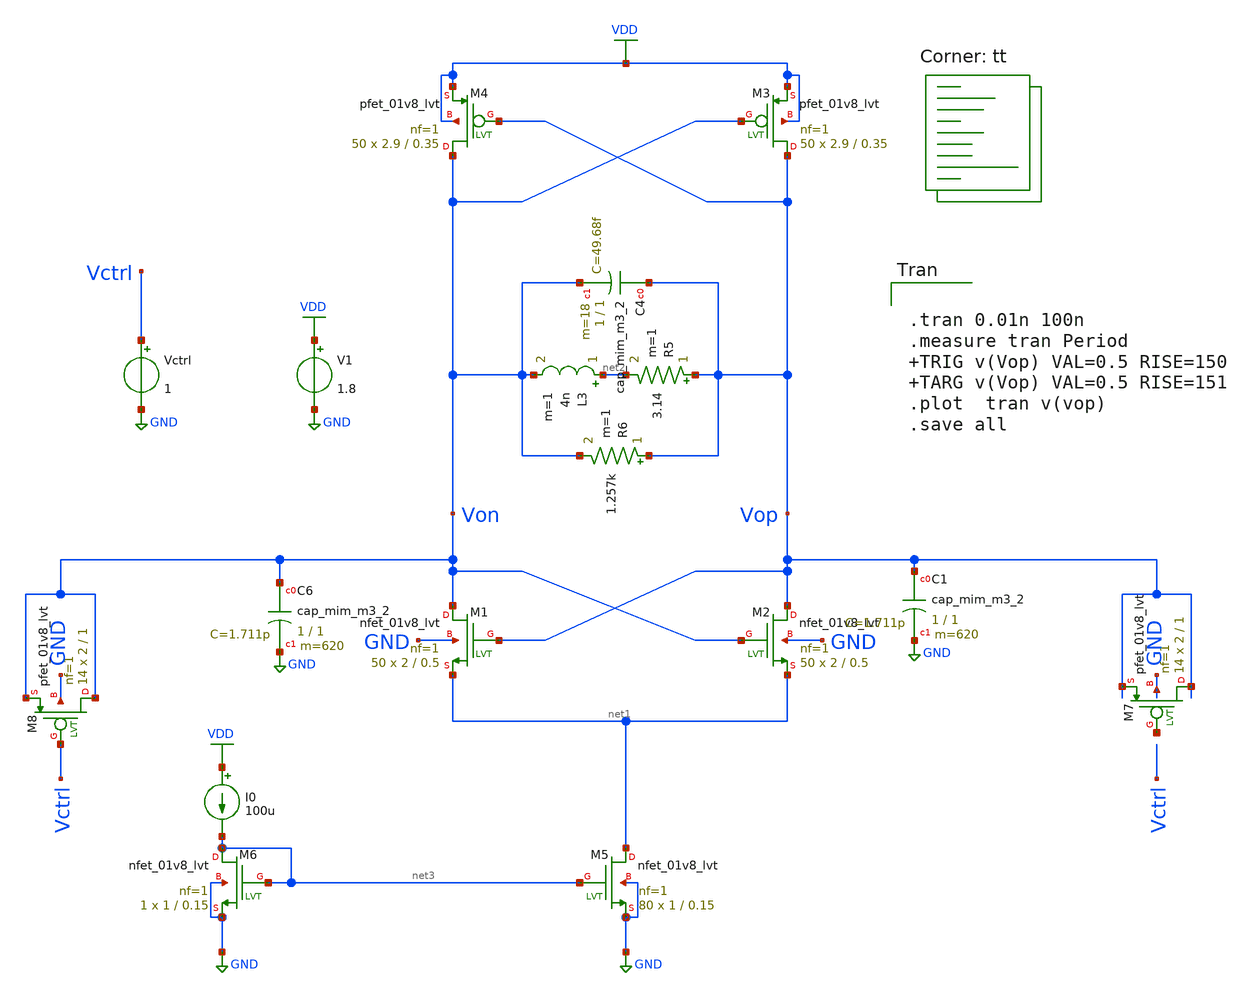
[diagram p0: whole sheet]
** sch_path: pll/lc_vco_lib/5_lc_vco_Hossam_Tarek/xschem/lc_osc_complementary.sch
**.subckt lc_osc_complementary
XM1 Von Vop net1 GND sky130_fd_pr__nfet_01v8_lvt L=0.5 W=2 nf=1 ad='int((nf+1)/2) * W/nf * 0.29' as='int((nf+2)/2) * W/nf * 0.29'
+ pd='2*int((nf+1)/2) * (W/nf + 0.29)' ps='2*int((nf+2)/2) * (W/nf + 0.29)' nrd='0.29 / W' nrs='0.29 / W'
+ sa=0 sb=0 sd=0 mult=50 m=50
XM2 Vop Von net1 GND sky130_fd_pr__nfet_01v8_lvt L=0.5 W=2 nf=1 ad='int((nf+1)/2) * W/nf * 0.29' as='int((nf+2)/2) * W/nf * 0.29'
+ pd='2*int((nf+1)/2) * (W/nf + 0.29)' ps='2*int((nf+2)/2) * (W/nf + 0.29)' nrd='0.29 / W' nrs='0.29 / W'
+ sa=0 sb=0 sd=0 mult=50 m=50
V1 VDD GND 1.8
XC6 Von GND sky130_fd_pr__cap_mim_m3_2 W=1 L=1 MF=620 m=620
XC1 Vop GND sky130_fd_pr__cap_mim_m3_2 W=1 L=1 MF=620 m=620
L3 net2 Von 4n m=1
R5 Vop net2 3.14 m=1
R6 Vop Von 1.257k m=1
XC4 Vop Von sky130_fd_pr__cap_mim_m3_2 W=1 L=1 MF=18 m=18
XM3 Vop Von VDD VDD sky130_fd_pr__pfet_01v8_lvt L=0.35 W=2.9 nf=1 ad='int((nf+1)/2) * W/nf * 0.29' as='int((nf+2)/2) * W/nf * 0.29'
+ pd='2*int((nf+1)/2) * (W/nf + 0.29)' ps='2*int((nf+2)/2) * (W/nf + 0.29)' nrd='0.29 / W' nrs='0.29 / W'
+ sa=0 sb=0 sd=0 mult=50 m=50
XM4 Von Vop VDD VDD sky130_fd_pr__pfet_01v8_lvt L=0.35 W=2.9 nf=1 ad='int((nf+1)/2) * W/nf * 0.29' as='int((nf+2)/2) * W/nf * 0.29'
+ pd='2*int((nf+1)/2) * (W/nf + 0.29)' ps='2*int((nf+2)/2) * (W/nf + 0.29)' nrd='0.29 / W' nrs='0.29 / W'
+ sa=0 sb=0 sd=0 mult=50 m=50
XM5 net1 net3 GND GND sky130_fd_pr__nfet_01v8_lvt L=0.15 W=1 nf=1 ad='int((nf+1)/2) * W/nf * 0.29' as='int((nf+2)/2) * W/nf * 0.29'
+ pd='2*int((nf+1)/2) * (W/nf + 0.29)' ps='2*int((nf+2)/2) * (W/nf + 0.29)' nrd='0.29 / W' nrs='0.29 / W'
+ sa=0 sb=0 sd=0 mult=80 m=80
XM6 net3 net3 GND GND sky130_fd_pr__nfet_01v8_lvt L=0.15 W=1 nf=1 ad='int((nf+1)/2) * W/nf * 0.29' as='int((nf+2)/2) * W/nf * 0.29'
+ pd='2*int((nf+1)/2) * (W/nf + 0.29)' ps='2*int((nf+2)/2) * (W/nf + 0.29)' nrd='0.29 / W' nrs='0.29 / W'
+ sa=0 sb=0 sd=0 mult=1 m=1
I0 VDD net3 100u
XM7 Vop net4 Vop GND sky130_fd_pr__pfet_01v8_lvt L=1 W=2 nf=1 ad='int((nf+1)/2) * W/nf * 0.29' as='int((nf+2)/2) * W/nf * 0.29'
+ pd='2*int((nf+1)/2) * (W/nf + 0.29)' ps='2*int((nf+2)/2) * (W/nf + 0.29)' nrd='0.29 / W' nrs='0.29 / W'
+ sa=0 sb=0 sd=0 mult=14 m=14
XM8 Von Vctrl Von GND sky130_fd_pr__pfet_01v8_lvt L=1 W=2 nf=1 ad='int((nf+1)/2) * W/nf * 0.29' as='int((nf+2)/2) * W/nf * 0.29'
+ pd='2*int((nf+1)/2) * (W/nf + 0.29)' ps='2*int((nf+2)/2) * (W/nf + 0.29)' nrd='0.29 / W' nrs='0.29 / W'
+ sa=0 sb=0 sd=0 mult=14 m=14
Vctrl Vctrl GND 1
**** begin user architecture code


.tran 0.01n 100n
.measure tran Period  TRIG v(Vop) VAL=0.5 RISE=150 TARG v(Vop) VAL=0.5 RISE=151
.plot  tran v(vop)
.save all

.lib $::SKYWATER_MODELS/sky130.lib.spice tt
**** end user architecture code
**.ends
.GLOBAL GND
.GLOBAL VDD
.end
